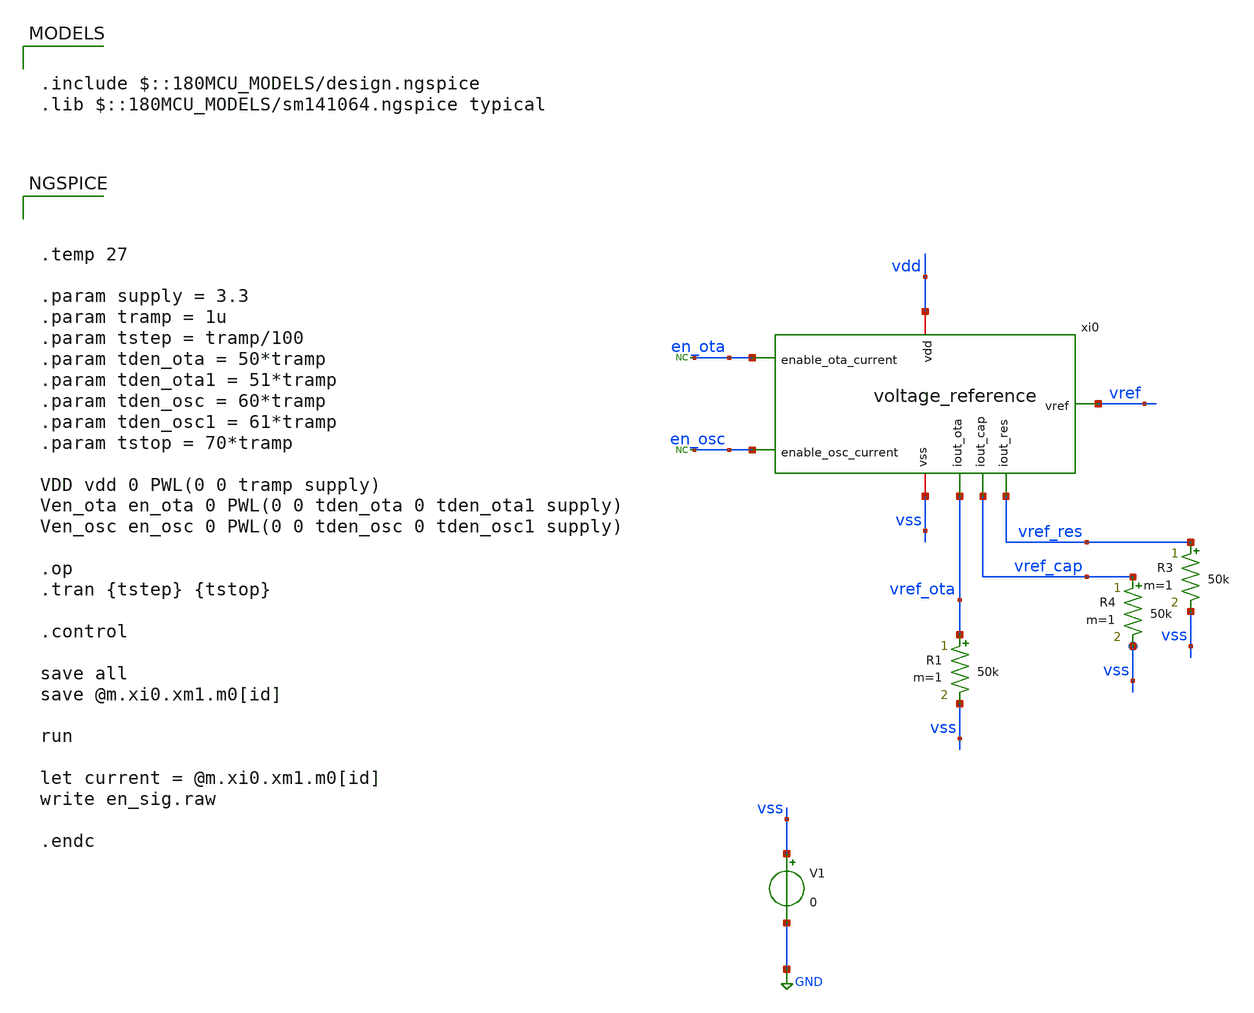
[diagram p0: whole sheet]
** sch_path: DESIGN/DACFUTURE_EDU/Voltage_Reference/tb_reference.sch
**.subckt tb_reference
xi0 vss vdd en_ota en_osc vref_cap vref_res vref_ota vref voltage_reference
V1 vss GND 0
R1 vref_ota vss 50k m=1
R3 vref_res vss 50k m=1
R4 vref_cap vss 50k m=1
* noconn en_ota
* noconn en_osc
**** begin user architecture code

.include $::180MCU_MODELS/design.ngspice
.lib $::180MCU_MODELS/sm141064.ngspice typical




.temp 27

.param supply = 3.3
.param tramp = 1u
.param tstep = tramp/100
.param tden_ota = 50*tramp
.param tden_ota1 = 51*tramp
.param tden_osc = 60*tramp
.param tden_osc1 = 61*tramp
.param tstop = 70*tramp

VDD vdd 0 PWL(0 0 tramp supply)
Ven_ota en_ota 0 PWL(0 0 tden_ota 0 tden_ota1 supply)
Ven_osc en_osc 0 PWL(0 0 tden_osc 0 tden_osc1 supply)

.op
.tran {tstep} {tstop}

.control

save all
save @m.xi0.xm1.m0[id]

run

let current = @m.xi0.xm1.m0[id]
write en_sig.raw

.endc



**** end user architecture code
**.ends
.GLOBAL GND
.end
